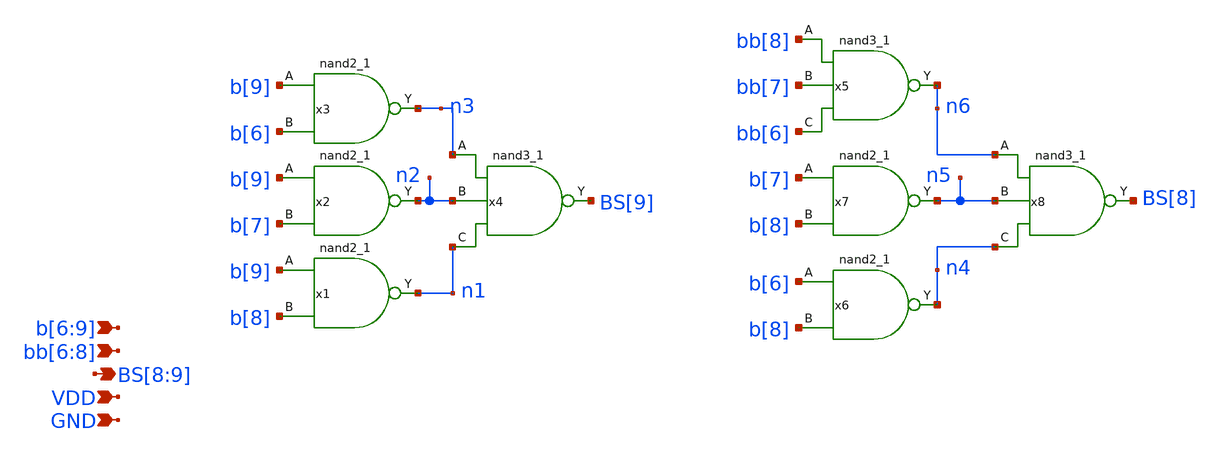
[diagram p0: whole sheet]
** sch_path: xschem/logic_shift_seg2.sch
**.subckt logic_shift_seg2 b[6],b[7],b[8],b[9] BS[8],BS[9] GND VDD bb[6],bb[7],bb[8]
*.ipin b[6],b[7],b[8],b[9]
*.opin BS[8],BS[9]
*.ipin GND
*.ipin VDD
*.ipin bb[6],bb[7],bb[8]
x1 b[9] b[8] GND GND VDD VDD n1 sky130_fd_sc_hd__nand2_1
x2 b[9] b[7] GND GND VDD VDD n2 sky130_fd_sc_hd__nand2_1
x3 b[9] b[6] GND GND VDD VDD n3 sky130_fd_sc_hd__nand2_1
x5 bb[8] bb[7] bb[6] GND GND VDD VDD n6 sky130_fd_sc_hd__nand3_1
x4 n3 n2 n1 GND GND VDD VDD BS[9] sky130_fd_sc_hd__nand3_1
x6 b[6] b[8] GND GND VDD VDD n4 sky130_fd_sc_hd__nand2_1
x7 b[7] b[8] GND GND VDD VDD n5 sky130_fd_sc_hd__nand2_1
x8 n6 n5 n4 GND GND VDD VDD BS[8] sky130_fd_sc_hd__nand3_1
**.ends
.end
